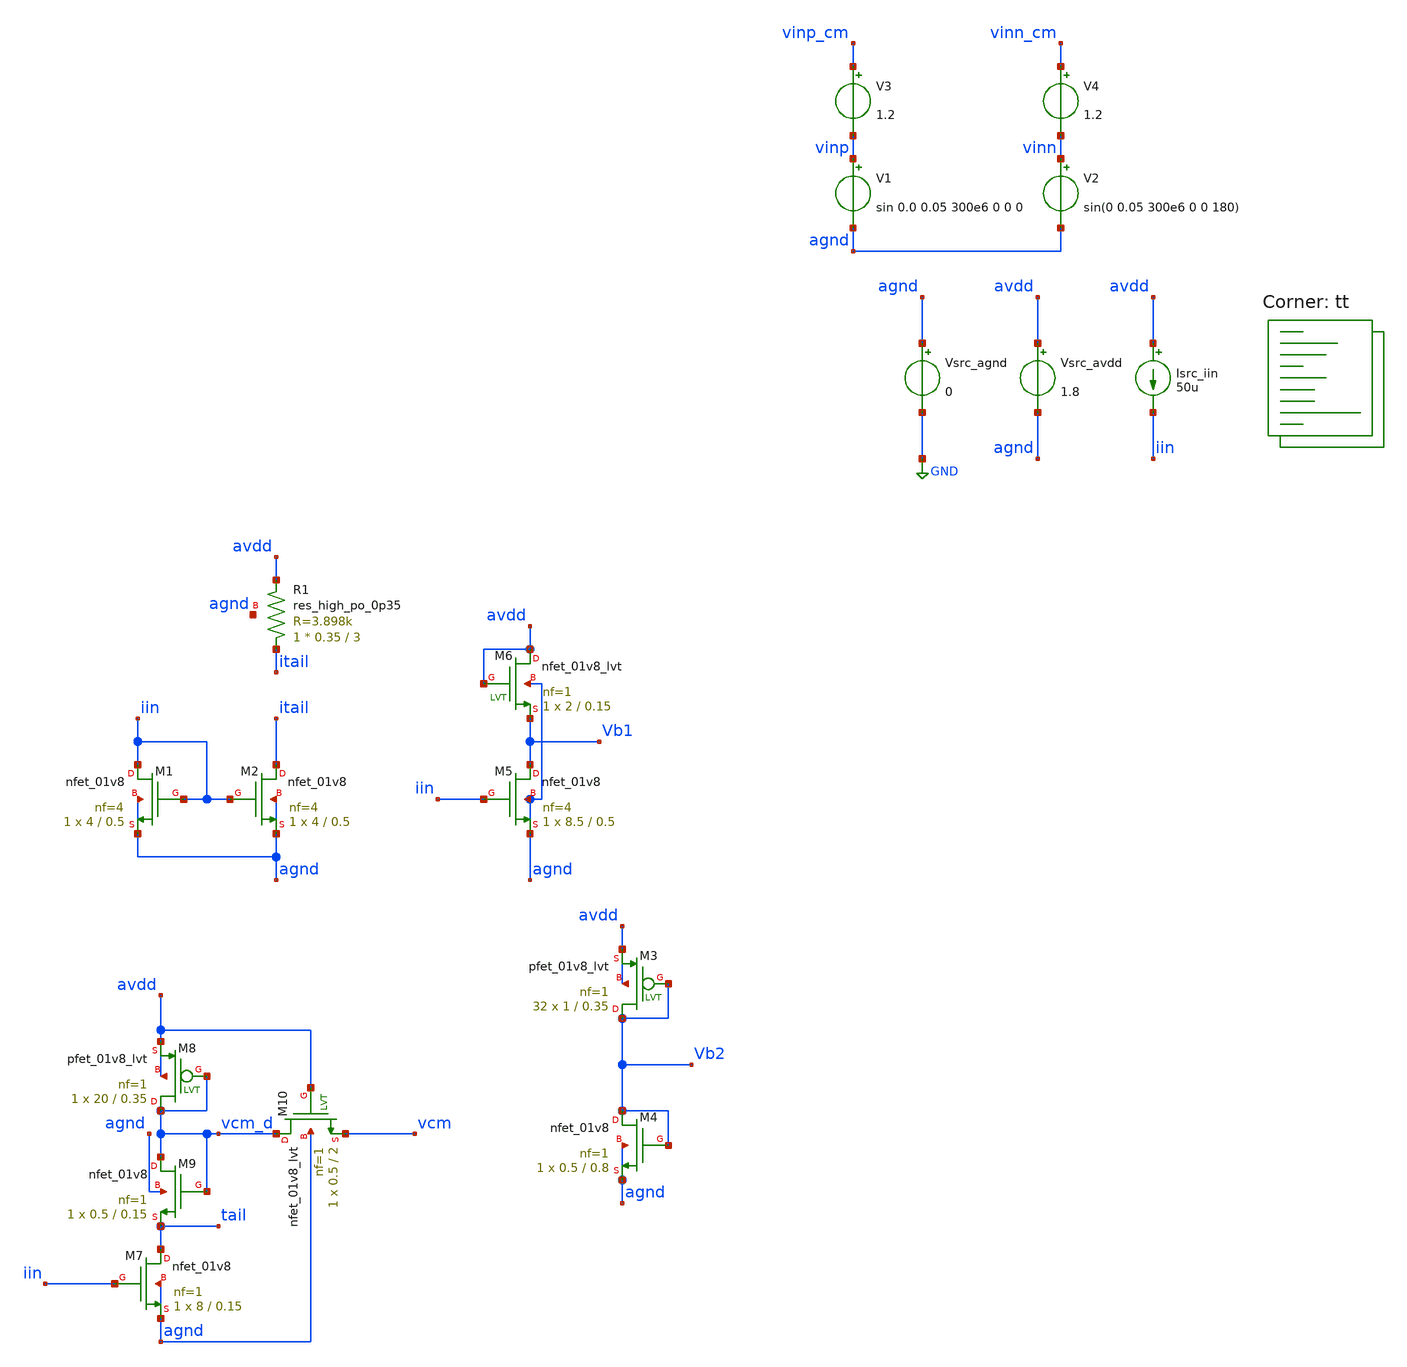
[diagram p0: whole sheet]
** sch_path: AMP/TB_Biases.sch
**.subckt TB_Biases
Vsrc_agnd agnd GND 0
Vsrc_avdd avdd agnd 1.8
Isrc_iin avdd iin 50u
XM1 iin iin agnd agnd sky130_fd_pr__nfet_01v8 L=0.5 W=4 nf=4 ad='int((nf+1)/2) * W/nf * 0.29' as='int((nf+2)/2) * W/nf * 0.29'
+ pd='2*int((nf+1)/2) * (W/nf + 0.29)' ps='2*int((nf+2)/2) * (W/nf + 0.29)' nrd='0.29 / W' nrs='0.29 / W'
+ sa=0 sb=0 sd=0 mult=1 m=1
XM2 itail iin agnd agnd sky130_fd_pr__nfet_01v8 L=0.5 W=4 nf=4 ad='int((nf+1)/2) * W/nf * 0.29' as='int((nf+2)/2) * W/nf * 0.29'
+ pd='2*int((nf+1)/2) * (W/nf + 0.29)' ps='2*int((nf+2)/2) * (W/nf + 0.29)' nrd='0.29 / W' nrs='0.29 / W'
+ sa=0 sb=0 sd=0 mult=1 m=1
XR1 itail avdd agnd sky130_fd_pr__res_high_po_0p35 L=3 mult=1 m=1
XM5 Vb1 iin agnd agnd sky130_fd_pr__nfet_01v8 L=0.5 W=8.5 nf=4 ad='int((nf+1)/2) * W/nf * 0.29' as='int((nf+2)/2) * W/nf * 0.29'
+ pd='2*int((nf+1)/2) * (W/nf + 0.29)' ps='2*int((nf+2)/2) * (W/nf + 0.29)' nrd='0.29 / W' nrs='0.29 / W'
+ sa=0 sb=0 sd=0 mult=1 m=1
XM6 avdd avdd Vb1 agnd sky130_fd_pr__nfet_01v8_lvt L=0.15 W=2 nf=1 ad='int((nf+1)/2) * W/nf * 0.29' as='int((nf+2)/2) * W/nf * 0.29'
+ pd='2*int((nf+1)/2) * (W/nf + 0.29)' ps='2*int((nf+2)/2) * (W/nf + 0.29)' nrd='0.29 / W' nrs='0.29 / W'
+ sa=0 sb=0 sd=0 mult=1 m=1
XM7 tail iin agnd agnd sky130_fd_pr__nfet_01v8 L=0.15 W=8 nf=1 ad='int((nf+1)/2) * W/nf * 0.29' as='int((nf+2)/2) * W/nf * 0.29'
+ pd='2*int((nf+1)/2) * (W/nf + 0.29)' ps='2*int((nf+2)/2) * (W/nf + 0.29)' nrd='0.29 / W' nrs='0.29 / W'
+ sa=0 sb=0 sd=0 mult=1 m=1
XM9 vcm_d vcm_d tail agnd sky130_fd_pr__nfet_01v8 L=0.15 W=0.5 nf=1 ad='int((nf+1)/2) * W/nf * 0.29'
+ as='int((nf+2)/2) * W/nf * 0.29' pd='2*int((nf+1)/2) * (W/nf + 0.29)' ps='2*int((nf+2)/2) * (W/nf + 0.29)'
+ nrd='0.29 / W' nrs='0.29 / W' sa=0 sb=0 sd=0 mult=1 m=1
V3 vinp_cm vinp 1.2
V4 vinn_cm vinn 1.2
V1 vinp agnd sin 0.0 0.05 300e6 0 0 0
V2 vinn agnd sin(0 0.05 300e6 0 0 180)
XM8 vcm_d vcm_d avdd avdd sky130_fd_pr__pfet_01v8_lvt L=0.35 W=20 nf=1 ad='int((nf+1)/2) * W/nf * 0.29'
+ as='int((nf+2)/2) * W/nf * 0.29' pd='2*int((nf+1)/2) * (W/nf + 0.29)' ps='2*int((nf+2)/2) * (W/nf + 0.29)'
+ nrd='0.29 / W' nrs='0.29 / W' sa=0 sb=0 sd=0 mult=1 m=1
XM10 vcm_d avdd vcm agnd sky130_fd_pr__nfet_01v8_lvt L=2 W=0.5 nf=1 ad='int((nf+1)/2) * W/nf * 0.29'
+ as='int((nf+2)/2) * W/nf * 0.29' pd='2*int((nf+1)/2) * (W/nf + 0.29)' ps='2*int((nf+2)/2) * (W/nf + 0.29)'
+ nrd='0.29 / W' nrs='0.29 / W' sa=0 sb=0 sd=0 mult=1 m=1
XM3 Vb2 Vb2 avdd avdd sky130_fd_pr__pfet_01v8_lvt L=0.35 W=1 nf=1 ad='int((nf+1)/2) * W/nf * 0.29' as='int((nf+2)/2) * W/nf * 0.29'
+ pd='2*int((nf+1)/2) * (W/nf + 0.29)' ps='2*int((nf+2)/2) * (W/nf + 0.29)' nrd='0.29 / W' nrs='0.29 / W'
+ sa=0 sb=0 sd=0 mult=32 m=32
XM4 Vb2 Vb2 agnd agnd sky130_fd_pr__nfet_01v8 L=0.8 W=0.5 nf=1 ad='int((nf+1)/2) * W/nf * 0.29' as='int((nf+2)/2) * W/nf * 0.29'
+ pd='2*int((nf+1)/2) * (W/nf + 0.29)' ps='2*int((nf+2)/2) * (W/nf + 0.29)' nrd='0.29 / W' nrs='0.29 / W'
+ sa=0 sb=0 sd=0 mult=1 m=1
**** begin user architecture code

* this option enables mos model bin
* selection based on W/NF instead of W

.option savecurrents

.control
save all
op

* Print newline
echo

set nmos_list = ( xm1 xm2 xm7 xm9 xm5 xm4  )
set pmos_list = (  )
set nmos_lvt_list = ( xm6 xm10 )
set pmos_lvt_list = ( xm8 xm3 )

* Print stats for each MOSFET
foreach nmos $nmos_list
 * Save stats
 save @m.{$nmos}.msky130_fd_pr__nfet_01v8[gm]
 let vth   = @m.{$nmos}.msky130_fd_pr__nfet_01v8[vth]
 let vgs   = @m.{$nmos}.msky130_fd_pr__nfet_01v8[vgs]
 let vds   = @m.{$nmos}.msky130_fd_pr__nfet_01v8[vds]
 let vdsat = @m.{$nmos}.msky130_fd_pr__nfet_01v8[vdsat]
 let gm    = @m.{$nmos}.msky130_fd_pr__nfet_01v8[gm]
 let gds   = @m.{$nmos}.msky130_fd_pr__nfet_01v8[gds]


 * Print stats
 echo Stats for $nmos:
 print vth
 print vgs
 print vds
 print vdsat
 print gm
 print gds

 * Print newline
 echo
end

foreach pmos $pmos_list
 * Save stats
 save @m.{$pmos}.msky130_fd_pr__nfet_01v8[gm]
 let vth   = @m.{$pmos}.msky130_fd_pr__pfet_01v8[vth]
 let vgs   = @m.{$pmos}.msky130_fd_pr__pfet_01v8[vgs]
 let vds   = @m.{$pmos}.msky130_fd_pr__pfet_01v8[vds]
 let vdsat = @m.{$pmos}.msky130_fd_pr__pfet_01v8[vdsat]
 let gm    = @m.{$pmos}.msky130_fd_pr__pfet_01v8[gm]
 let gds   = @m.{$pmos}.msky130_fd_pr__pfet_01v8[gds]

 * Print stats
 echo Stats for $pmos:
 print vth
 print vgs
 print vds
 print vdsat
 print gm
 print gds

 * Print newline
 echo
end

foreach nmos_lvt $nmos_lvt_list
 * Save stats
 save @m.{$nmos_lvt}.msky130_fd_pr__nfet_01v8_lvt[gm]
 let vth   = @m.{$nmos_lvt}.msky130_fd_pr__nfet_01v8_lvt[vth]
 let vgs   = @m.{$nmos_lvt}.msky130_fd_pr__nfet_01v8_lvt[vgs]
 let vds   = @m.{$nmos_lvt}.msky130_fd_pr__nfet_01v8_lvt[vds]
 let vdsat = @m.{$nmos_lvt}.msky130_fd_pr__nfet_01v8_lvt[vdsat]
 let gm    = @m.{$nmos_lvt}.msky130_fd_pr__nfet_01v8_lvt[gm]
 let gds   = @m.{$nmos_lvt}.msky130_fd_pr__nfet_01v8_lvt[gds]


 * Print stats
 echo Stats for $nmos_lvt:
 print vth
 print vgs
 print vds
 print vdsat
 print gm
 print gds

 * Print newline
 echo
end

foreach pmos_lvt $pmos_lvt_list
 * Save stats
 save @m.{$pmos_lvt}.msky130_fd_pr__nfet_01v8_lvt[gm]
 let vth   = @m.{$pmos_lvt}.msky130_fd_pr__pfet_01v8_lvt[vth]
 let vgs   = @m.{$pmos_lvt}.msky130_fd_pr__pfet_01v8_lvt[vgs]
 let vds   = @m.{$pmos_lvt}.msky130_fd_pr__pfet_01v8_lvt[vds]
 let vdsat = @m.{$pmos_lvt}.msky130_fd_pr__pfet_01v8_lvt[vdsat]
 let gm    = @m.{$pmos_lvt}.msky130_fd_pr__pfet_01v8_lvt[gm]
 let gds   = @m.{$pmos_lvt}.msky130_fd_pr__pfet_01v8_lvt[gds]


 * Print stats
 echo Stats for $pmos_lvt:
 print vth
 print vgs
 print vds
 print vdsat
 print gm
 print gds

 * Print newline
 echo
end

* Print region of operation
echo Regions of Operation:
echo

echo NMOS:
foreach nmos $nmos_list
 * Save stats
 let vds = @m.{$nmos}.msky130_fd_pr__nfet_01v8[vds]
 let vgs = @m.{$nmos}.msky130_fd_pr__nfet_01v8[vgs]
 let vth = @m.{$nmos}.msky130_fd_pr__nfet_01v8[vth]

 * Check and print regions
 if (vgs <= vth)
  echo $nmos: N Cutoff
  print vgs
  print vth
 end
 if (vgs > vth) & (vds <= (vgs - vth))
  echo $nmos: N Triode
  print vgs
  print vth
  print vds
 end
 if (vgs > vth) & (vds > (vgs - vth))
  echo $nmos: N Saturation
 end
end
echo

echo PMOS:
foreach pmos $pmos_list
 * Save stats
 let vds = @m.{$pmos}.msky130_fd_pr__pfet_01v8[vds]
 let vgs = @m.{$pmos}.msky130_fd_pr__pfet_01v8[vgs]
 let vth = @m.{$pmos}.msky130_fd_pr__pfet_01v8[vth]

 * Check and print regions
 if (abs(vgs) <= abs(vth))
  echo $pmos: P Cutoff
  print vgs
  print vth
 end
 if (abs(vgs) > abs(vth)) & (abs(vds) <= (abs(vgs) - abs(vth)))
  echo $pmos: P Triode
  print vgs
  print vth
  print vds
 end
 if (abs(vgs) > abs(vth)) & (abs(vds) > (abs(vgs) - abs(vth)))
  echo $pmos: P Saturation
 end
end
echo

echo NMOS_lvt:
foreach nmos_lvt $nmos_lvt_list
 * Save stats
 let vds = @m.{$nmos_lvt}.msky130_fd_pr__nfet_01v8_lvt[vds]
 let vgs = @m.{$nmos_lvt}.msky130_fd_pr__nfet_01v8_lvt[vgs]
 let vth = @m.{$nmos_lvt}.msky130_fd_pr__nfet_01v8_lvt[vth]

 * Check and print regions
 if (vgs <= vth)
  echo $nmos_lvt: N Cutoff
  print vgs
  print vth
 end
 if (vgs > vth) & (vds <= (vgs - vth))
  echo $nmos_lvt: N Triode
  print vgs
  print vth
  print vds
 end
 if (vgs > vth) & (vds > (vgs - vth))
  echo $nmos_lvt: N Saturation
 end
end
echo

echo PMOS_lvt:
foreach pmos_lvt $pmos_lvt_list
 * Save stats
 let vds = @m.{$pmos_lvt}.msky130_fd_pr__pfet_01v8_lvt[vds]
 let vgs = @m.{$pmos_lvt}.msky130_fd_pr__pfet_01v8_lvt[vgs]
 let vth = @m.{$pmos_lvt}.msky130_fd_pr__pfet_01v8_lvt[vth]

 * Check and print regions
 if (abs(vgs) <= abs(vth))
  echo $pmos_lvt: P Cutoff
  print vgs
  print vth
 end
 if (abs(vgs) > abs(vth)) & (abs(vds) <= (abs(vgs) - abs(vth)))
  echo $pmos_lvt: P Triode
  print vgs
  print vth
  print vds
 end
 if (abs(vgs) > abs(vth)) & (abs(vds) > (abs(vgs) - abs(vth)))
  echo $pmos_lvt: P Saturation
 end
end
echo

* Allow biases to settle
*tran 0.002n 30n
*plot vinn vinp vinn_cm vinp_cm vcm Vb1

save all
write TB_Biases.raw
set appendwrite

.endc


.lib $::SKYWATER_MODELS/sky130.lib.spice tt
**** end user architecture code
**.ends
.GLOBAL GND
.end
